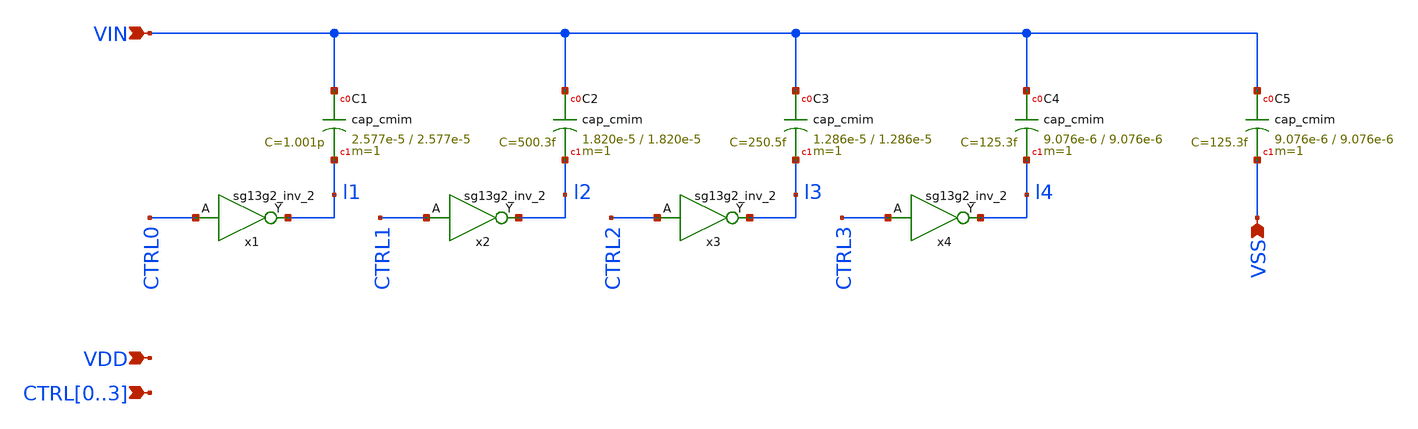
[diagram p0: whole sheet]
** sch_path: designs/cdac/cdac.sch
* IHP-GmbH/IHP-Open-PDK/ihp-sg13g2/libs.tech/xschem/sg13g2_stdcells/sg13g2_inv_2.sch:
* Copyright 2023 IHP PDK Authors
* Licensed under the Apache License, Version 2.0 (the "License");
**.subckt cdac VIN CTRL0,CTRL1,CTRL2,CTRL3 VSS VDD
*.ipin VIN
*.ipin CTRL0,CTRL1,CTRL2,CTRL3
*.ipin VSS
*.ipin VDD
XC1 VIN l1 cap_cmim w=2.577e-5 l=2.577e-5 m=1 mm_ok=1
XC2 VIN l2 cap_cmim w=1.820e-5 l=1.820e-5 m=1 mm_ok=1
XC3 VIN l3 cap_cmim w=1.286e-5 l=1.286e-5 m=1 mm_ok=1
XC4 VIN l4 cap_cmim w=9.076e-6 l=9.076e-6 m=1 mm_ok=1
XC5 VIN VSS cap_cmim w=9.076e-6 l=9.076e-6 m=1 mm_ok=1
x1 l1 CTRL0 VDD VSS sg13g2_inv_2
x2 l2 CTRL1 VDD VSS sg13g2_inv_2
x3 l3 CTRL2 VDD VSS sg13g2_inv_2
x4 l4 CTRL3 VDD VSS sg13g2_inv_2
**.ends

* expanding   symbol:  sg13g2_stdcells/sg13g2_inv_2.sym # of pins=2
** sym_path: sg13g2_stdcells/sg13g2_inv_2.sym
** sch_path: sg13g2_stdcells/sg13g2_inv_2.sch
.subckt sg13g2_inv_2 Y A VDD VSS
*.opin Y
*.ipin A
*.iopin VDD
*.iopin VSS
XM1 Y A VSS VSS sg13_lv_nmos w=1.48u l=130.00n ng=2 m=1 mm_ok=1
XM2 Y A VDD VDD sg13_lv_pmos w=2.24u l=130.00n ng=2 m=1 mm_ok=1
.ends

.end
